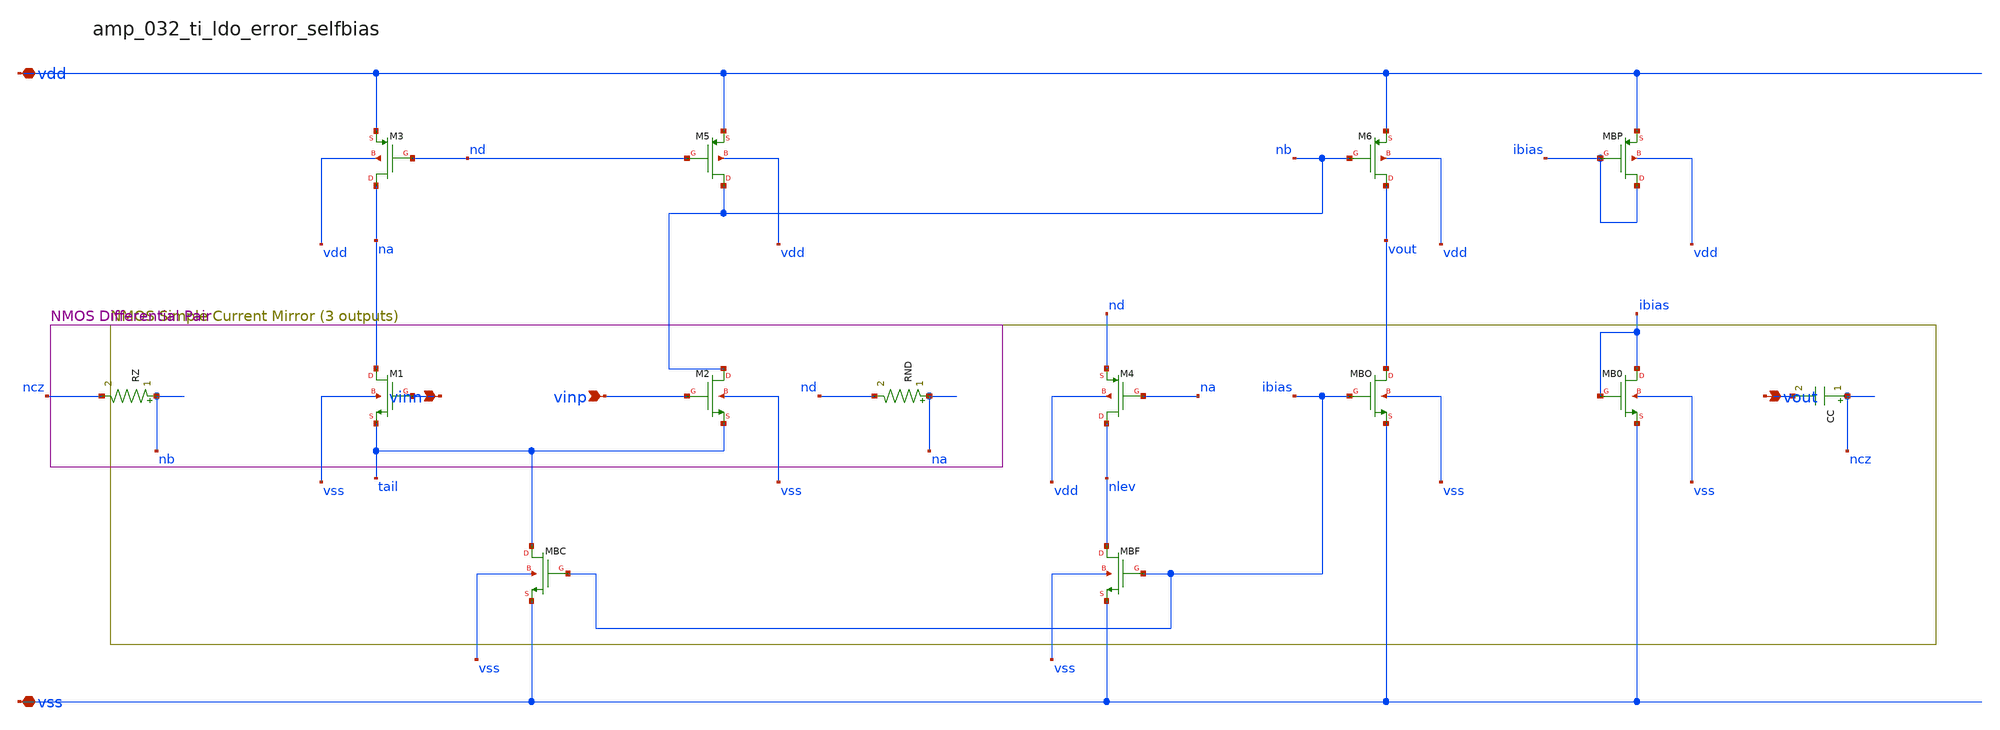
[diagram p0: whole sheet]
** sch_path: analog-db/raw/amp_032_ti_ldo_error_selfbias/amp_032_ti_ldo_error_selfbias_annotated.sch
**.subckt amp_032_ti_ldo_error_selfbias_annotated vinn vinp vdd vss vout
*.ipin vinn
*.ipin vinp
*.iopin vdd
*.iopin vss
*.opin vout
CC ncz vout 'c_comp' m=1
RND na nd 'r_nd' m=1
RZ nb ncz 'r_z' m=1
XM1 na vinn tail vss sg13_lv_nmos w=x_dut_xm1_w l=x_dut_xm1_l ng=1 m=1
XM2 nb vinp tail vss sg13_lv_nmos w=x_dut_xm2_w l=x_dut_xm2_l ng=1 m=1
XM3 na nd vdd vdd sg13_lv_pmos w=x_dut_xm3_w l=x_dut_xm3_l ng=1 m=1
XM4 nlev na nd vdd sg13_lv_pmos w=x_dut_xm4_w l=x_dut_xm4_l ng=1 m=1
XM5 nb nd vdd vdd sg13_lv_pmos w=x_dut_xm5_w l=x_dut_xm5_l ng=1 m=1
XM6 vout nb vdd vdd sg13_lv_pmos w=x_dut_xm6_w l=x_dut_xm6_l ng=1 m=1
XMB0 ibias ibias vss vss sg13_lv_nmos w=x_dut_xmb0_w l=x_dut_xmb0_l ng=1 m=1
XMBC tail ibias vss vss sg13_lv_nmos w=x_dut_xmbc_w l=x_dut_xmbc_l ng=1 m=x_dut_xmbc_m
XMBF nlev ibias vss vss sg13_lv_nmos w=x_dut_xmbf_w l=x_dut_xmbf_l ng=1 m=1
XMBO vout ibias vss vss sg13_lv_nmos w=x_dut_xmbo_w l=x_dut_xmbo_l ng=1 m=x_dut_xmbo_m
XMBP ibias ibias vdd vdd sg13_lv_pmos w=x_dut_xmbp_w l=x_dut_xmbp_l ng=1 m=1
**.ends
.end
